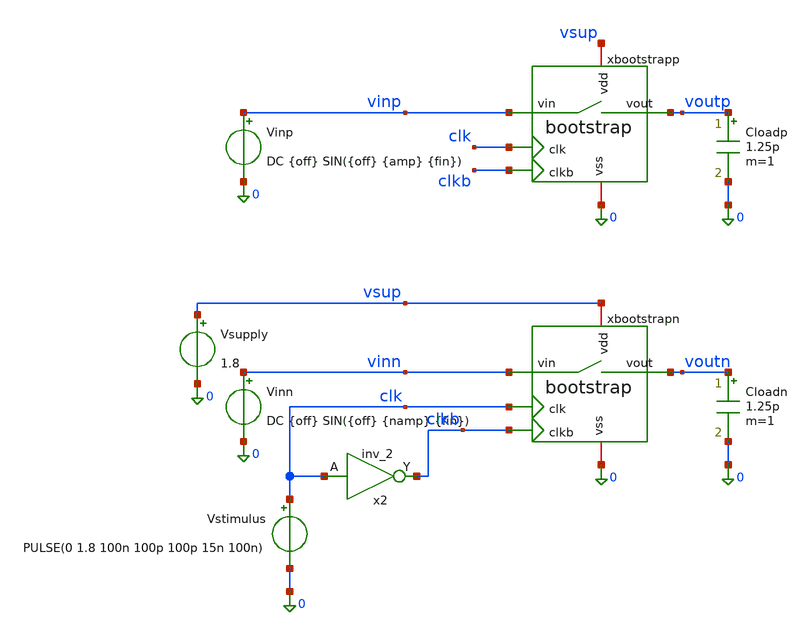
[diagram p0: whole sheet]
** sch_path: xschem/sar-adc_tb/tb3_THD.sch
.lib $::SKYWATER_MODELS/sky130.lib.spice tt
.include $::SKYWATER_STDCELLS/sky130_fd_sc_hd.spice

**.subckt tb3_THD
xbootstrapn clk clkb vinn voutn vsup 0 bootstrap
Vstimulus clk 0 PULSE(0 1.8 100n 100p 100p 15n 100n)
Vsupply vsup 0 1.8
Vinn vinn 0 DC {off} SIN({off} {namp} {fin})
x2 clk 0 0 vsup vsup clkb sky130_fd_sc_hd__inv_2
xbootstrapp clk clkb vinp voutp vsup 0 bootstrap
Vinp vinp 0 DC {off} SIN({off} {amp} {fin})
Cloadp voutp 0 1.25p m=1
Cloadn voutn 0 1.25p m=1
**** begin user architecture code


.control
  tran 50p 6.6u
  setplot $curplot

  echo ''
  echo '=== TB3  sampel keluaran (dibaca thd.py) ========================'
  let k = 0
  dowhile k < 64
    let tk = 120e-9 + k*100e-9
    meas tran sp FIND v(voutp) AT=$&tk
    meas tran sn FIND v(voutn) AT=$&tk
    meas tran ip FIND v(vinp)  AT=$&tk
    echo 'SAMPLE $&k $&sp $&sn $&ip'
    let k = k + 1
  end
  echo '=== akhir sampel ================================================'
  echo ''

  write tb3_thd.raw
.endc




.param nfft = 64
.param mcyc = 29
.param fs = 10e6
.param fin  = 'mcyc/nfft*fs'     $ 4.53125 MHz
.param amp  = 0.88               $ hampir full-scale single-ended
.param off  = 0.9                $ V_CM
.param namp = '-amp'             $ amplitudo sisi n (fase berlawanan)
.options reltol=1e-4 vntol=1e-8 abstol=1e-14 chgtol=1e-16


**** end user architecture code
**.ends

* expanding   symbol:  bootstrap.sym # of pins=6
** sym_path: xschem/sar-adc/bootstrap.sym
** sch_path: xschem/sar-adc/bootstrap.sch
.subckt bootstrap clk clkb vin vout vdd vss
*.ipin clk
*.ipin clkb
*.ipin vin
*.opin vout
*.iopin vdd
*.iopin vss
XMswitch vin vgate vout vss sky130_fd_pr__nfet_01v8 L=0.15 W=2 nf=1 ad='int((1 + 1)/2) * 2 / 1 * 0.29'
+ as='int((1 + 2)/2) * 2 / 1 * 0.29' pd='2*int((1 + 1)/2) * (2 / 1 + 0.29)' ps='2*int((1 + 2)/2) * (2 / 1 + 0.29)'
+ nrd='0.29 / 2 ' nrs='0.29 / 2 ' sa=0 sb=0 sd=0 mult=1 m=1
XMdisbot cbot vgate vin vss sky130_fd_pr__nfet_01v8 L=0.15 W=1 nf=1 ad='int((1 + 1)/2) * 1 / 1 * 0.29'
+ as='int((1 + 2)/2) * 1 / 1 * 0.29' pd='2*int((1 + 1)/2) * (1 / 1 + 0.29)' ps='2*int((1 + 2)/2) * (1 / 1 + 0.29)'
+ nrd='0.29 / 1 ' nrs='0.29 / 1 ' sa=0 sb=0 sd=0 mult=1 m=1
XCboot ctop cbot sky130_fd_pr__cap_mim_m3_1 W=10 L=10 MF=1 m=1
XMdistop vgate vgdistop ctop ctop sky130_fd_pr__pfet_01v8 L=0.15 W=1 nf=1 ad='int((1 + 1)/2) * 1 / 1 * 0.29'
+ as='int((1 + 2)/2) * 1 / 1 * 0.29' pd='2*int((1 + 1)/2) * (1 / 1 + 0.29)' ps='2*int((1 + 2)/2) * (1 / 1 + 0.29)'
+ nrd='0.29 / 1 ' nrs='0.29 / 1 ' sa=0 sb=0 sd=0 mult=1 m=1
XMchtop ctop vgate vdd ctop sky130_fd_pr__pfet_01v8 L=0.15 W=1 nf=1 ad='int((1 + 1)/2) * 1 / 1 * 0.29'
+ as='int((1 + 2)/2) * 1 / 1 * 0.29' pd='2*int((1 + 1)/2) * (1 / 1 + 0.29)' ps='2*int((1 + 2)/2) * (1 / 1 + 0.29)'
+ nrd='0.29 / 1 ' nrs='0.29 / 1 ' sa=0 sb=0 sd=0 mult=1 m=1
XMdistopdrv vgdistop vgate cbot vss sky130_fd_pr__nfet_01v8 L=0.15 W=0.5 nf=1 ad='int((1 + 1)/2) * 0.5 / 1 * 0.29'
+ as='int((1 + 2)/2) * 0.5 / 1 * 0.29' pd='2*int((1 + 1)/2) * (0.5 / 1 + 0.29)' ps='2*int((1 + 2)/2) * (0.5 / 1 + 0.29)'
+ nrd='0.29 / 0.5 ' nrs='0.29 / 0.5 ' sa=0 sb=0 sd=0 mult=1 m=1
XMchtopdrv2 vschtopdrv1 clkb vss vss sky130_fd_pr__nfet_01v8 L=0.15 W=1 nf=1 ad='int((1 + 1)/2) * 1 / 1 * 0.29'
+ as='int((1 + 2)/2) * 1 / 1 * 0.29' pd='2*int((1 + 1)/2) * (1 / 1 + 0.29)' ps='2*int((1 + 2)/2) * (1 / 1 + 0.29)'
+ nrd='0.29 / 1 ' nrs='0.29 / 1 ' sa=0 sb=0 sd=0 mult=1 m=1
XMchbot cbot clkb vss vss sky130_fd_pr__nfet_01v8 L=0.15 W=1 nf=1 ad='int((1 + 1)/2) * 1 / 1 * 0.29'
+ as='int((1 + 2)/2) * 1 / 1 * 0.29' pd='2*int((1 + 1)/2) * (1 / 1 + 0.29)' ps='2*int((1 + 2)/2) * (1 / 1 + 0.29)'
+ nrd='0.29 / 1 ' nrs='0.29 / 1 ' sa=0 sb=0 sd=0 mult=1 m=1
XM1 vgdistop clk vdd vdd sky130_fd_pr__pfet_01v8 L=0.15 W=1 nf=1 ad='int((1 + 1)/2) * 1 / 1 * 0.29' as='int((1 + 2)/2) * 1 / 1 * 0.29'
+ pd='2*int((1 + 1)/2) * (1 / 1 + 0.29)' ps='2*int((1 + 2)/2) * (1 / 1 + 0.29)' nrd='0.29 / 1 ' nrs='0.29 / 1 '
+ sa=0 sb=0 sd=0 mult=1 m=1
XM2 vgdistop clk cbot vss sky130_fd_pr__nfet_01v8 L=0.15 W=0.5 nf=1 ad='int((1 + 1)/2) * 0.5 / 1 * 0.29'
+ as='int((1 + 2)/2) * 0.5 / 1 * 0.29' pd='2*int((1 + 1)/2) * (0.5 / 1 + 0.29)' ps='2*int((1 + 2)/2) * (0.5 / 1 + 0.29)'
+ nrd='0.29 / 0.5 ' nrs='0.29 / 0.5 ' sa=0 sb=0 sd=0 mult=1 m=1
XXMchtopdrv1 vgate vdd vschtopdrv1 vss sky130_fd_pr__nfet_g5v0d10v5 L=0.5 W=3 nf=1 ad='int((1 + 1)/2) * 3 / 1 * 0.29'
+ as='int((1 + 2)/2) * 3 / 1 * 0.29' pd='2*int((1 + 1)/2) * (3 / 1 + 0.29)' ps='2*int((1 + 2)/2) * (3 / 1 + 0.29)'
+ nrd='0.29 / 3 ' nrs='0.29 / 3 ' sa=0 sb=0 sd=0 mult=1 m=1
.ends

.end
